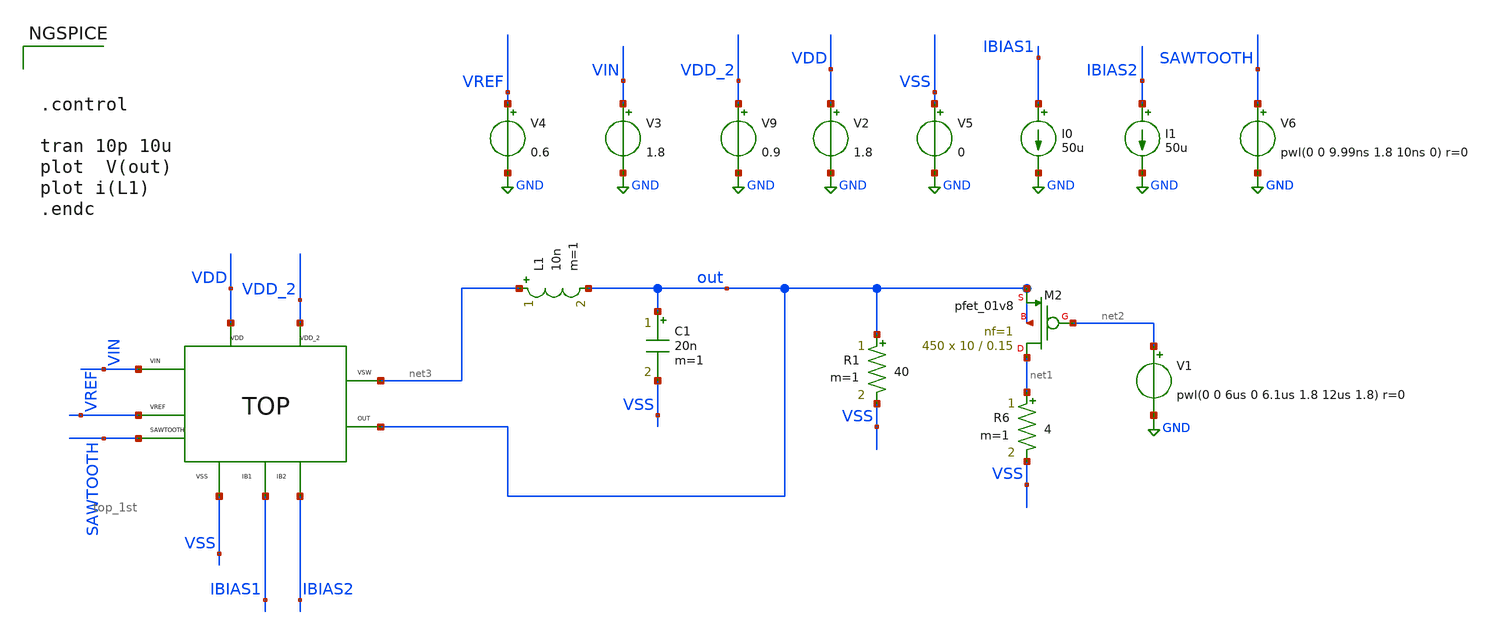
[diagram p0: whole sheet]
** sch_path: xschem/DC_DC_Converter_xschem/OTHERS/DC_DC_Converter_2/DC_DC_Converter/TOP_LEVEL/Top_Final/top_1st_TB.sch
**.subckt top_1st_TB
L1 net3 out 10n m=1
C1 out VSS 20n m=1
V3 VIN GND 1.8
I0 IBIAS1 GND 50u
V9 VDD_2 GND 0.9
V2 VDD GND 1.8
V5 VSS GND 0
V4 VREF GND 0.6
I1 IBIAS2 GND 50u
V6 SAWTOOTH GND pwl(0 0 9.99ns 1.8 10ns 0) r=0
R1 out VSS 40 m=1
XM2 net1 net2 out out sky130_fd_pr__pfet_01v8 L=0.15 W=10 nf=1 ad='int((nf+1)/2) * W/nf * 0.29' as='int((nf+2)/2) * W/nf * 0.29'
+ pd='2*int((nf+1)/2) * (W/nf + 0.29)' ps='2*int((nf+2)/2) * (W/nf + 0.29)' nrd='0.29 / W' nrs='0.29 / W'
+ sa=0 sb=0 sd=0 mult=450 m=450
R6 net1 VSS 4 m=1
V1 net2 GND pwl(0 0 6us 0 6.1us 1.8 12us 1.8) r=0
XM1 VDD VDD_2 net3 out VIN VREF SAWTOOTH VSS IBIAS1 IBIAS2 top_1st
**** begin user architecture code

** opencircuitdesign pdks install
.lib $::SKYWATER_MODELS/sky130.lib.spice tt





.control

tran 10p 10u
plot  V(out)
plot i(L1)
.endc


**** end user architecture code
**.ends
.GLOBAL GND
.end
